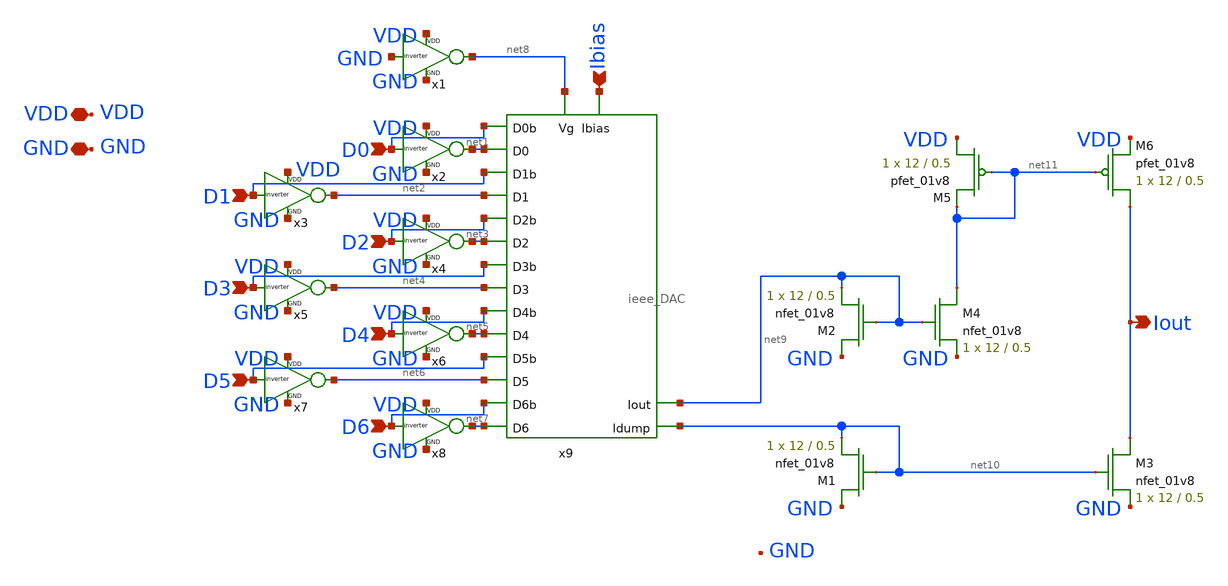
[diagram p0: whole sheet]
** sch_path: schematics/ieee DAC/ieee_simple_M_2M_DAC_with_subtractor.sch
**.subckt ieee_simple_M_2M_DAC_with_subtractor Ibias Iout D0 D1 D2 D3 D4 D5 D6 VDD GND
*.ipin Ibias
*.opin Iout
*.ipin D0
*.ipin D1
*.ipin D2
*.ipin D3
*.ipin D4
*.ipin D5
*.ipin D6
*.iopin VDD
*.iopin GND
x1 VDD GND net8 GND inverter
x2 VDD D0 net1 GND inverter
x3 VDD D1 net2 GND inverter
x4 VDD D2 net3 GND inverter
x5 VDD D3 net4 GND inverter
x6 VDD D4 net5 GND inverter
x7 VDD D5 net6 GND inverter
x8 VDD D6 net7 GND inverter
x9 Ibias net8 net1 net3 net4 net5 net6 D5 net2 D0 D1 D2 D3 D4 net7 D6 net9 net10 ieee_DAC
XM1 GND net10 net10 GND sky130_fd_pr__nfet_01v8 L=0.5 W=12 nf=1 ad='int((nf+1)/2) * W/nf * 0.29' as='int((nf+2)/2) * W/nf * 0.29'
+ pd='2*int((nf+1)/2) * (W/nf + 0.29)' ps='2*int((nf+2)/2) * (W/nf + 0.29)' nrd='0.29 / W' nrs='0.29 / W'
+ sa=0 sb=0 sd=0 mult=1 m=1
XM2 GND net9 net9 GND sky130_fd_pr__nfet_01v8 L=0.5 W=12 nf=1 ad='int((nf+1)/2) * W/nf * 0.29' as='int((nf+2)/2) * W/nf * 0.29'
+ pd='2*int((nf+1)/2) * (W/nf + 0.29)' ps='2*int((nf+2)/2) * (W/nf + 0.29)' nrd='0.29 / W' nrs='0.29 / W'
+ sa=0 sb=0 sd=0 mult=1 m=1
XM3 Iout net10 GND GND sky130_fd_pr__nfet_01v8 L=0.5 W=12 nf=1 ad='int((nf+1)/2) * W/nf * 0.29' as='int((nf+2)/2) * W/nf * 0.29'
+ pd='2*int((nf+1)/2) * (W/nf + 0.29)' ps='2*int((nf+2)/2) * (W/nf + 0.29)' nrd='0.29 / W' nrs='0.29 / W'
+ sa=0 sb=0 sd=0 mult=1 m=1
XM4 net11 net9 GND GND sky130_fd_pr__nfet_01v8 L=0.5 W=12 nf=1 ad='int((nf+1)/2) * W/nf * 0.29' as='int((nf+2)/2) * W/nf * 0.29'
+ pd='2*int((nf+1)/2) * (W/nf + 0.29)' ps='2*int((nf+2)/2) * (W/nf + 0.29)' nrd='0.29 / W' nrs='0.29 / W'
+ sa=0 sb=0 sd=0 mult=1 m=1
XM5 VDD net11 net11 VDD sky130_fd_pr__pfet_01v8 L=0.5 W=12 nf=1 ad='int((nf+1)/2) * W/nf * 0.29' as='int((nf+2)/2) * W/nf * 0.29'
+ pd='2*int((nf+1)/2) * (W/nf + 0.29)' ps='2*int((nf+2)/2) * (W/nf + 0.29)' nrd='0.29 / W' nrs='0.29 / W'
+ sa=0 sb=0 sd=0 mult=1 m=1
XM6 Iout net11 VDD VDD sky130_fd_pr__pfet_01v8 L=0.5 W=12 nf=1 ad='int((nf+1)/2) * W/nf * 0.29' as='int((nf+2)/2) * W/nf * 0.29'
+ pd='2*int((nf+1)/2) * (W/nf + 0.29)' ps='2*int((nf+2)/2) * (W/nf + 0.29)' nrd='0.29 / W' nrs='0.29 / W'
+ sa=0 sb=0 sd=0 mult=1 m=1
**.ends

* expanding   symbol:  /home/madvlsi/dev/git/7-bit-D-A-converter-MP4-MADVLSI/schematics/ieee
*+ DAC/inverter.sym # of pins=4
** sym_path: schematics/ieee DAC/inverter.sym
** sch_path: schematics/ieee DAC/inverter.sch
.subckt inverter VDD A Y GND
*.ipin A
*.iopin VDD
*.iopin GND
*.opin Y
XM1 Y A GND GND sky130_fd_pr__nfet_01v8 L=0.5 W=12 nf=1 ad='int((nf+1)/2) * W/nf * 0.29' as='int((nf+2)/2) * W/nf * 0.29'
+ pd='2*int((nf+1)/2) * (W/nf + 0.29)' ps='2*int((nf+2)/2) * (W/nf + 0.29)' nrd='0.29 / W' nrs='0.29 / W'
+ sa=0 sb=0 sd=0 mult=1 m=1
XM2 Y A VDD VDD sky130_fd_pr__pfet_01v8 L=0.5 W=12 nf=1 ad='int((nf+1)/2) * W/nf * 0.29' as='int((nf+2)/2) * W/nf * 0.29'
+ pd='2*int((nf+1)/2) * (W/nf + 0.29)' ps='2*int((nf+2)/2) * (W/nf + 0.29)' nrd='0.29 / W' nrs='0.29 / W'
+ sa=0 sb=0 sd=0 mult=1 m=1
.ends


* expanding   symbol:  /home/madvlsi/dev/git/7-bit-D-A-converter-MP4-MADVLSI/schematics/ieee
*+ DAC/ieee_DAC.sym # of pins=18
** sym_path: schematics/ieee DAC/ieee_DAC.sym
** sch_path: schematics/ieee DAC/ieee_DAC.sch
.subckt ieee_DAC Ibias Vg D0 D2 D3 D4 D5 D5b D1 D0b D1b D2b D3b D4b D6 D6b Iout Idump
*.ipin D0
*.ipin D1
*.ipin D2
*.ipin D3
*.ipin D4
*.ipin D5
*.ipin D6
*.ipin D0b
*.ipin D1b
*.ipin D2b
*.ipin D3b
*.ipin D4b
*.ipin D5b
*.ipin D6b
*.iopin Iout
*.iopin Idump
*.iopin Ibias
*.iopin Vg
XM1 Ibias Vg net12 GND sky130_fd_pr__nfet_01v8 L=0.5 W=12 nf=1 ad='int((nf+1)/2) * W/nf * 0.29' as='int((nf+2)/2) * W/nf * 0.29'
+ pd='2*int((nf+1)/2) * (W/nf + 0.29)' ps='2*int((nf+2)/2) * (W/nf + 0.29)' nrd='0.29 / W' nrs='0.29 / W'
+ sa=0 sb=0 sd=0 mult=1 m=1
XM4 Ibias Vg net1 GND sky130_fd_pr__nfet_01v8 L=0.5 W=12 nf=1 ad='int((nf+1)/2) * W/nf * 0.29' as='int((nf+2)/2) * W/nf * 0.29'
+ pd='2*int((nf+1)/2) * (W/nf + 0.29)' ps='2*int((nf+2)/2) * (W/nf + 0.29)' nrd='0.29 / W' nrs='0.29 / W'
+ sa=0 sb=0 sd=0 mult=1 m=1
XM5 net1 Vg net11 GND sky130_fd_pr__nfet_01v8 L=0.5 W=12 nf=1 ad='int((nf+1)/2) * W/nf * 0.29' as='int((nf+2)/2) * W/nf * 0.29'
+ pd='2*int((nf+1)/2) * (W/nf + 0.29)' ps='2*int((nf+2)/2) * (W/nf + 0.29)' nrd='0.29 / W' nrs='0.29 / W'
+ sa=0 sb=0 sd=0 mult=1 m=1
XM8 net1 Vg net2 GND sky130_fd_pr__nfet_01v8 L=0.5 W=12 nf=1 ad='int((nf+1)/2) * W/nf * 0.29' as='int((nf+2)/2) * W/nf * 0.29'
+ pd='2*int((nf+1)/2) * (W/nf + 0.29)' ps='2*int((nf+2)/2) * (W/nf + 0.29)' nrd='0.29 / W' nrs='0.29 / W'
+ sa=0 sb=0 sd=0 mult=1 m=1
XM9 net2 Vg net10 GND sky130_fd_pr__nfet_01v8 L=0.5 W=12 nf=1 ad='int((nf+1)/2) * W/nf * 0.29' as='int((nf+2)/2) * W/nf * 0.29'
+ pd='2*int((nf+1)/2) * (W/nf + 0.29)' ps='2*int((nf+2)/2) * (W/nf + 0.29)' nrd='0.29 / W' nrs='0.29 / W'
+ sa=0 sb=0 sd=0 mult=1 m=1
XM12 net2 Vg net3 GND sky130_fd_pr__nfet_01v8 L=0.5 W=12 nf=1 ad='int((nf+1)/2) * W/nf * 0.29' as='int((nf+2)/2) * W/nf * 0.29'
+ pd='2*int((nf+1)/2) * (W/nf + 0.29)' ps='2*int((nf+2)/2) * (W/nf + 0.29)' nrd='0.29 / W' nrs='0.29 / W'
+ sa=0 sb=0 sd=0 mult=1 m=1
XM13 net3 Vg net9 GND sky130_fd_pr__nfet_01v8 L=0.5 W=12 nf=1 ad='int((nf+1)/2) * W/nf * 0.29' as='int((nf+2)/2) * W/nf * 0.29'
+ pd='2*int((nf+1)/2) * (W/nf + 0.29)' ps='2*int((nf+2)/2) * (W/nf + 0.29)' nrd='0.29 / W' nrs='0.29 / W'
+ sa=0 sb=0 sd=0 mult=1 m=1
XM16 net3 Vg net4 GND sky130_fd_pr__nfet_01v8 L=0.5 W=12 nf=1 ad='int((nf+1)/2) * W/nf * 0.29' as='int((nf+2)/2) * W/nf * 0.29'
+ pd='2*int((nf+1)/2) * (W/nf + 0.29)' ps='2*int((nf+2)/2) * (W/nf + 0.29)' nrd='0.29 / W' nrs='0.29 / W'
+ sa=0 sb=0 sd=0 mult=1 m=1
XM17 net4 Vg net8 GND sky130_fd_pr__nfet_01v8 L=0.5 W=12 nf=1 ad='int((nf+1)/2) * W/nf * 0.29' as='int((nf+2)/2) * W/nf * 0.29'
+ pd='2*int((nf+1)/2) * (W/nf + 0.29)' ps='2*int((nf+2)/2) * (W/nf + 0.29)' nrd='0.29 / W' nrs='0.29 / W'
+ sa=0 sb=0 sd=0 mult=1 m=1
XM7 net4 Vg net5 GND sky130_fd_pr__nfet_01v8 L=0.5 W=12 nf=1 ad='int((nf+1)/2) * W/nf * 0.29' as='int((nf+2)/2) * W/nf * 0.29'
+ pd='2*int((nf+1)/2) * (W/nf + 0.29)' ps='2*int((nf+2)/2) * (W/nf + 0.29)' nrd='0.29 / W' nrs='0.29 / W'
+ sa=0 sb=0 sd=0 mult=1 m=1
XM10 net5 Vg net7 GND sky130_fd_pr__nfet_01v8 L=0.5 W=12 nf=1 ad='int((nf+1)/2) * W/nf * 0.29' as='int((nf+2)/2) * W/nf * 0.29'
+ pd='2*int((nf+1)/2) * (W/nf + 0.29)' ps='2*int((nf+2)/2) * (W/nf + 0.29)' nrd='0.29 / W' nrs='0.29 / W'
+ sa=0 sb=0 sd=0 mult=1 m=1
XM15 net5 Vg net6 GND sky130_fd_pr__nfet_01v8 L=0.5 W=12 nf=1 ad='int((nf+1)/2) * W/nf * 0.29' as='int((nf+2)/2) * W/nf * 0.29'
+ pd='2*int((nf+1)/2) * (W/nf + 0.29)' ps='2*int((nf+2)/2) * (W/nf + 0.29)' nrd='0.29 / W' nrs='0.29 / W'
+ sa=0 sb=0 sd=0 mult=1 m=1
XM18 net6 Vg net13 GND sky130_fd_pr__nfet_01v8 L=0.5 W=12 nf=1 ad='int((nf+1)/2) * W/nf * 0.29' as='int((nf+2)/2) * W/nf * 0.29'
+ pd='2*int((nf+1)/2) * (W/nf + 0.29)' ps='2*int((nf+2)/2) * (W/nf + 0.29)' nrd='0.29 / W' nrs='0.29 / W'
+ sa=0 sb=0 sd=0 mult=1 m=1
XM2 net7 D5 Iout GND sky130_fd_pr__nfet_01v8 L=0.5 W=12 nf=1 ad='int((nf+1)/2) * W/nf * 0.29' as='int((nf+2)/2) * W/nf * 0.29'
+ pd='2*int((nf+1)/2) * (W/nf + 0.29)' ps='2*int((nf+2)/2) * (W/nf + 0.29)' nrd='0.29 / W' nrs='0.29 / W'
+ sa=0 sb=0 sd=0 mult=1 m=1
XM3 Idump D5b net7 GND sky130_fd_pr__nfet_01v8 L=0.5 W=12 nf=1 ad='int((nf+1)/2) * W/nf * 0.29' as='int((nf+2)/2) * W/nf * 0.29'
+ pd='2*int((nf+1)/2) * (W/nf + 0.29)' ps='2*int((nf+2)/2) * (W/nf + 0.29)' nrd='0.29 / W' nrs='0.29 / W'
+ sa=0 sb=0 sd=0 mult=1 m=1
XM6 net8 D4 Iout GND sky130_fd_pr__nfet_01v8 L=0.5 W=12 nf=1 ad='int((nf+1)/2) * W/nf * 0.29' as='int((nf+2)/2) * W/nf * 0.29'
+ pd='2*int((nf+1)/2) * (W/nf + 0.29)' ps='2*int((nf+2)/2) * (W/nf + 0.29)' nrd='0.29 / W' nrs='0.29 / W'
+ sa=0 sb=0 sd=0 mult=1 m=1
XM11 Idump D4b net8 GND sky130_fd_pr__nfet_01v8 L=0.5 W=12 nf=1 ad='int((nf+1)/2) * W/nf * 0.29' as='int((nf+2)/2) * W/nf * 0.29'
+ pd='2*int((nf+1)/2) * (W/nf + 0.29)' ps='2*int((nf+2)/2) * (W/nf + 0.29)' nrd='0.29 / W' nrs='0.29 / W'
+ sa=0 sb=0 sd=0 mult=1 m=1
XM14 net9 D3 Iout GND sky130_fd_pr__nfet_01v8 L=0.5 W=12 nf=1 ad='int((nf+1)/2) * W/nf * 0.29' as='int((nf+2)/2) * W/nf * 0.29'
+ pd='2*int((nf+1)/2) * (W/nf + 0.29)' ps='2*int((nf+2)/2) * (W/nf + 0.29)' nrd='0.29 / W' nrs='0.29 / W'
+ sa=0 sb=0 sd=0 mult=1 m=1
XM19 Idump D3b net9 GND sky130_fd_pr__nfet_01v8 L=0.5 W=12 nf=1 ad='int((nf+1)/2) * W/nf * 0.29' as='int((nf+2)/2) * W/nf * 0.29'
+ pd='2*int((nf+1)/2) * (W/nf + 0.29)' ps='2*int((nf+2)/2) * (W/nf + 0.29)' nrd='0.29 / W' nrs='0.29 / W'
+ sa=0 sb=0 sd=0 mult=1 m=1
XM20 net10 D2 Iout GND sky130_fd_pr__nfet_01v8 L=0.5 W=12 nf=1 ad='int((nf+1)/2) * W/nf * 0.29' as='int((nf+2)/2) * W/nf * 0.29'
+ pd='2*int((nf+1)/2) * (W/nf + 0.29)' ps='2*int((nf+2)/2) * (W/nf + 0.29)' nrd='0.29 / W' nrs='0.29 / W'
+ sa=0 sb=0 sd=0 mult=1 m=1
XM21 Idump D2b net10 GND sky130_fd_pr__nfet_01v8 L=0.5 W=12 nf=1 ad='int((nf+1)/2) * W/nf * 0.29' as='int((nf+2)/2) * W/nf * 0.29'
+ pd='2*int((nf+1)/2) * (W/nf + 0.29)' ps='2*int((nf+2)/2) * (W/nf + 0.29)' nrd='0.29 / W' nrs='0.29 / W'
+ sa=0 sb=0 sd=0 mult=1 m=1
XM22 net11 D1 Iout GND sky130_fd_pr__nfet_01v8 L=0.5 W=12 nf=1 ad='int((nf+1)/2) * W/nf * 0.29' as='int((nf+2)/2) * W/nf * 0.29'
+ pd='2*int((nf+1)/2) * (W/nf + 0.29)' ps='2*int((nf+2)/2) * (W/nf + 0.29)' nrd='0.29 / W' nrs='0.29 / W'
+ sa=0 sb=0 sd=0 mult=1 m=1
XM23 Idump D1b net11 GND sky130_fd_pr__nfet_01v8 L=0.5 W=12 nf=1 ad='int((nf+1)/2) * W/nf * 0.29' as='int((nf+2)/2) * W/nf * 0.29'
+ pd='2*int((nf+1)/2) * (W/nf + 0.29)' ps='2*int((nf+2)/2) * (W/nf + 0.29)' nrd='0.29 / W' nrs='0.29 / W'
+ sa=0 sb=0 sd=0 mult=1 m=1
XM24 net12 D0 Iout GND sky130_fd_pr__nfet_01v8 L=0.5 W=12 nf=1 ad='int((nf+1)/2) * W/nf * 0.29' as='int((nf+2)/2) * W/nf * 0.29'
+ pd='2*int((nf+1)/2) * (W/nf + 0.29)' ps='2*int((nf+2)/2) * (W/nf + 0.29)' nrd='0.29 / W' nrs='0.29 / W'
+ sa=0 sb=0 sd=0 mult=1 m=1
XM25 Idump D0b net12 GND sky130_fd_pr__nfet_01v8 L=0.5 W=12 nf=1 ad='int((nf+1)/2) * W/nf * 0.29' as='int((nf+2)/2) * W/nf * 0.29'
+ pd='2*int((nf+1)/2) * (W/nf + 0.29)' ps='2*int((nf+2)/2) * (W/nf + 0.29)' nrd='0.29 / W' nrs='0.29 / W'
+ sa=0 sb=0 sd=0 mult=1 m=1
XM26 net13 D6 Iout GND sky130_fd_pr__nfet_01v8 L=0.5 W=12 nf=1 ad='int((nf+1)/2) * W/nf * 0.29' as='int((nf+2)/2) * W/nf * 0.29'
+ pd='2*int((nf+1)/2) * (W/nf + 0.29)' ps='2*int((nf+2)/2) * (W/nf + 0.29)' nrd='0.29 / W' nrs='0.29 / W'
+ sa=0 sb=0 sd=0 mult=1 m=1
XM27 Idump D6b net13 GND sky130_fd_pr__nfet_01v8 L=0.5 W=12 nf=1 ad='int((nf+1)/2) * W/nf * 0.29' as='int((nf+2)/2) * W/nf * 0.29'
+ pd='2*int((nf+1)/2) * (W/nf + 0.29)' ps='2*int((nf+2)/2) * (W/nf + 0.29)' nrd='0.29 / W' nrs='0.29 / W'
+ sa=0 sb=0 sd=0 mult=1 m=1
XM28 net6 Vg net14 GND sky130_fd_pr__nfet_01v8 L=0.5 W=12 nf=1 ad='int((nf+1)/2) * W/nf * 0.29' as='int((nf+2)/2) * W/nf * 0.29'
+ pd='2*int((nf+1)/2) * (W/nf + 0.29)' ps='2*int((nf+2)/2) * (W/nf + 0.29)' nrd='0.29 / W' nrs='0.29 / W'
+ sa=0 sb=0 sd=0 mult=1 m=1
XM29 net14 Vg Idump GND sky130_fd_pr__nfet_01v8 L=0.5 W=12 nf=1 ad='int((nf+1)/2) * W/nf * 0.29' as='int((nf+2)/2) * W/nf * 0.29'
+ pd='2*int((nf+1)/2) * (W/nf + 0.29)' ps='2*int((nf+2)/2) * (W/nf + 0.29)' nrd='0.29 / W' nrs='0.29 / W'
+ sa=0 sb=0 sd=0 mult=1 m=1
.ends

.end
